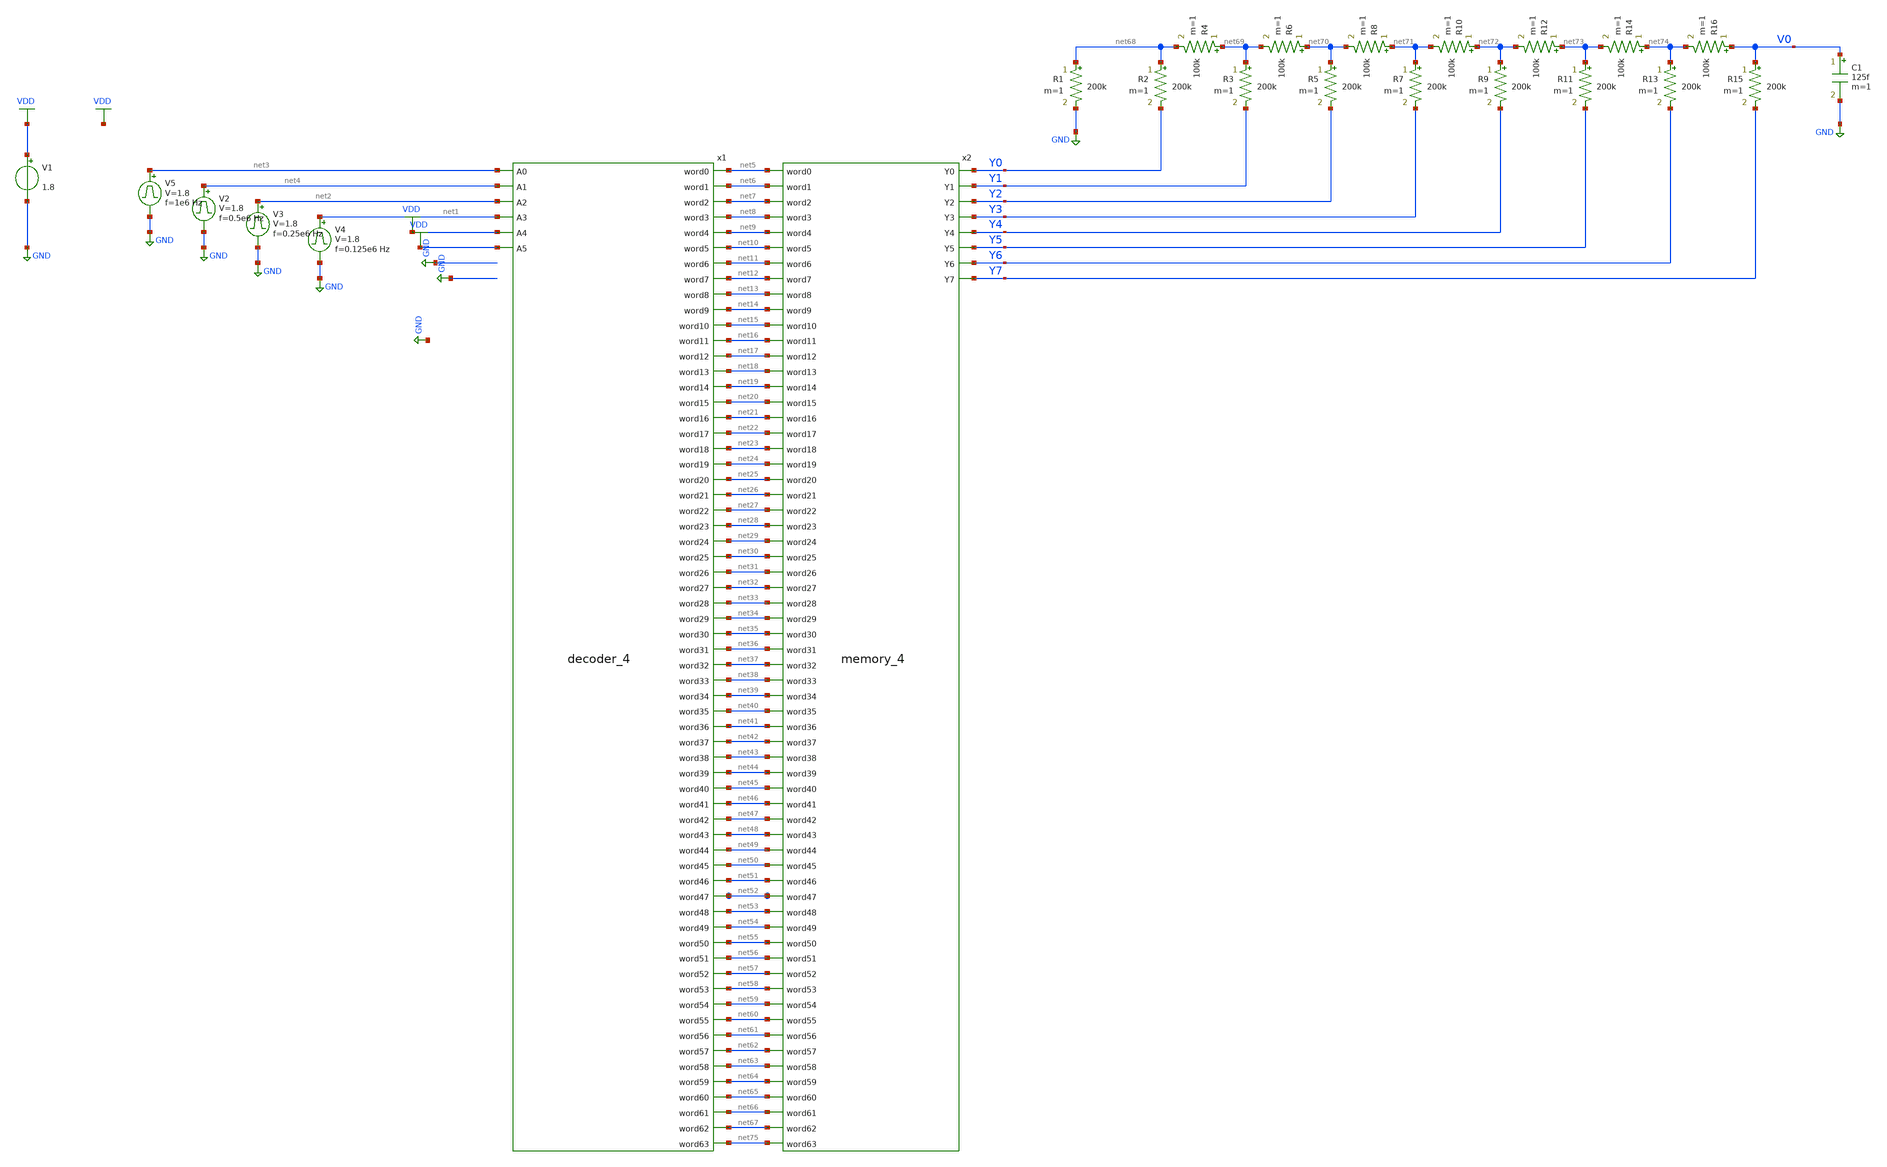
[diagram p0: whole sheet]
** sch_path: circuits/xschem/testing/decoder_memory_4_tb.sch
**.subckt decoder_memory_4_tb
V1 VDD GND 1.8
x1 net1 VDD net4 VDD net3 net2 net5 net6 net7 net8 net9 net10 net11 net12 net13 net14 net15 net16
+ net17 net18 net19 net20 net21 net22 net23 net24 net25 net26 net27 net28 net29 net30 net31 net32 net33
+ net34 net35 net36 net37 net38 net39 net40 net41 net42 net43 net44 net45 net46 net47 net48 net49 net50
+ net51 net52 net53 net54 net55 net56 net57 net58 net59 net60 net61 net62 net63 net64 net65 net66 net67
+ net75 decoder_4
x2 net5 net6 net7 net8 net9 net10 net11 net12 net13 net14 net15 net16 net17 net18 net19 net20 net21
+ net22 net23 net24 net25 net26 net27 net28 net29 net30 net31 net32 net33 net34 net35 net36 net37 net38
+ net39 net40 net41 net42 net43 net44 net45 net46 net47 net48 net49 net50 net51 net52 net53 net54 net55
+ net56 net57 net58 net59 net60 net61 net62 net63 net64 net65 net66 net67 net75 Y0 Y1 Y2 Y3 Y4 Y5 Y6 Y7
+ memory_4
V2 net4 GND pulse 0 1.8 '0.495/ 0.5e6 ' '0.01/0.5e6 ' '0.01/0.5e6 ' '0.49/0.5e6 ' '1/0.5e6 '
V3 net2 GND pulse 0 1.8 '0.495/ 0.25e6 ' '0.01/0.25e6 ' '0.01/0.25e6 ' '0.49/0.25e6 ' '1/0.25e6 '
V4 net1 GND pulse 0 1.8 '0.495/ 0.125e6 ' '0.01/0.125e6 ' '0.01/0.125e6 ' '0.49/0.125e6 ' '1/0.125e6 '
V5 net3 GND pulse 0 1.8 '0.495/ 1e6 ' '0.01/1e6 ' '0.01/1e6 ' '0.49/1e6 ' '1/1e6 '
R1 net68 GND 200k m=1
R2 net68 Y0 200k m=1
R3 net69 Y1 200k m=1
R4 net69 net68 100k m=1
R5 net70 Y2 200k m=1
R6 net70 net69 100k m=1
R7 net71 Y3 200k m=1
R8 net71 net70 100k m=1
R9 net72 Y4 200k m=1
R10 net72 net71 100k m=1
R11 net73 Y5 200k m=1
R12 net73 net72 100k m=1
R13 net74 Y6 200k m=1
R14 net74 net73 100k m=1
R15 V0 Y7 200k m=1
R16 V0 net74 100k m=1
C1 V0 GND 125f m=1
**** begin user architecture code


.control
save all
tran 1n 8u uic
plot V(V0)
.endc



** opencircuitdesign pdks install
.lib $::SKYWATER_MODELS/sky130.lib.spice tt


**** end user architecture code
**.ends
.GLOBAL VDD
.GLOBAL GND
.end
